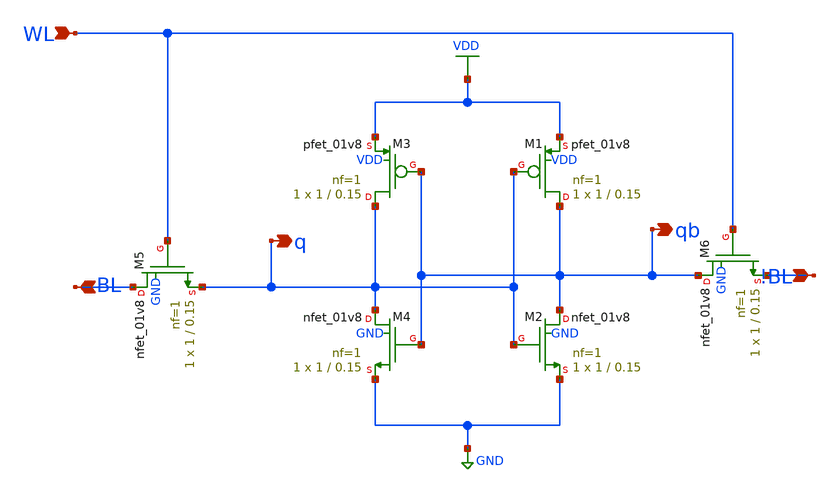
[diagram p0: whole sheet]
** sch_path: gates/Memory/1 bit 6-T SRAM.sch
**.subckt 1 bit 6-T SRAM WL BL !BL qb q
*.ipin WL
*.ipin BL
*.ipin !BL
*.opin qb
*.opin q
XM1 qb q VDD VDD sky130_fd_pr__pfet_01v8 L=0.15 W=1 nf=1 ad='int((nf+1)/2) * W/nf * 0.29' as='int((nf+2)/2) * W/nf * 0.29'
+ pd='2*int((nf+1)/2) * (W/nf + 0.29)' ps='2*int((nf+2)/2) * (W/nf + 0.29)' nrd='0.29 / W' nrs='0.29 / W'
+ sa=0 sb=0 sd=0 mult=1 m=1
XM2 qb q GND GND sky130_fd_pr__nfet_01v8 L=0.15 W=1 nf=1 ad='int((nf+1)/2) * W/nf * 0.29' as='int((nf+2)/2) * W/nf * 0.29'
+ pd='2*int((nf+1)/2) * (W/nf + 0.29)' ps='2*int((nf+2)/2) * (W/nf + 0.29)' nrd='0.29 / W' nrs='0.29 / W'
+ sa=0 sb=0 sd=0 mult=1 m=1
XM3 q qb VDD VDD sky130_fd_pr__pfet_01v8 L=0.15 W=1 nf=1 ad='int((nf+1)/2) * W/nf * 0.29' as='int((nf+2)/2) * W/nf * 0.29'
+ pd='2*int((nf+1)/2) * (W/nf + 0.29)' ps='2*int((nf+2)/2) * (W/nf + 0.29)' nrd='0.29 / W' nrs='0.29 / W'
+ sa=0 sb=0 sd=0 mult=1 m=1
XM4 q qb GND GND sky130_fd_pr__nfet_01v8 L=0.15 W=1 nf=1 ad='int((nf+1)/2) * W/nf * 0.29' as='int((nf+2)/2) * W/nf * 0.29'
+ pd='2*int((nf+1)/2) * (W/nf + 0.29)' ps='2*int((nf+2)/2) * (W/nf + 0.29)' nrd='0.29 / W' nrs='0.29 / W'
+ sa=0 sb=0 sd=0 mult=1 m=1
XM5 BL WL q GND sky130_fd_pr__nfet_01v8 L=0.15 W=1 nf=1 ad='int((nf+1)/2) * W/nf * 0.29' as='int((nf+2)/2) * W/nf * 0.29'
+ pd='2*int((nf+1)/2) * (W/nf + 0.29)' ps='2*int((nf+2)/2) * (W/nf + 0.29)' nrd='0.29 / W' nrs='0.29 / W'
+ sa=0 sb=0 sd=0 mult=1 m=1
XM6 qb WL !BL GND sky130_fd_pr__nfet_01v8 L=0.15 W=1 nf=1 ad='int((nf+1)/2) * W/nf * 0.29' as='int((nf+2)/2) * W/nf * 0.29'
+ pd='2*int((nf+1)/2) * (W/nf + 0.29)' ps='2*int((nf+2)/2) * (W/nf + 0.29)' nrd='0.29 / W' nrs='0.29 / W'
+ sa=0 sb=0 sd=0 mult=1 m=1
**.ends
.GLOBAL GND
.GLOBAL VDD
.end
